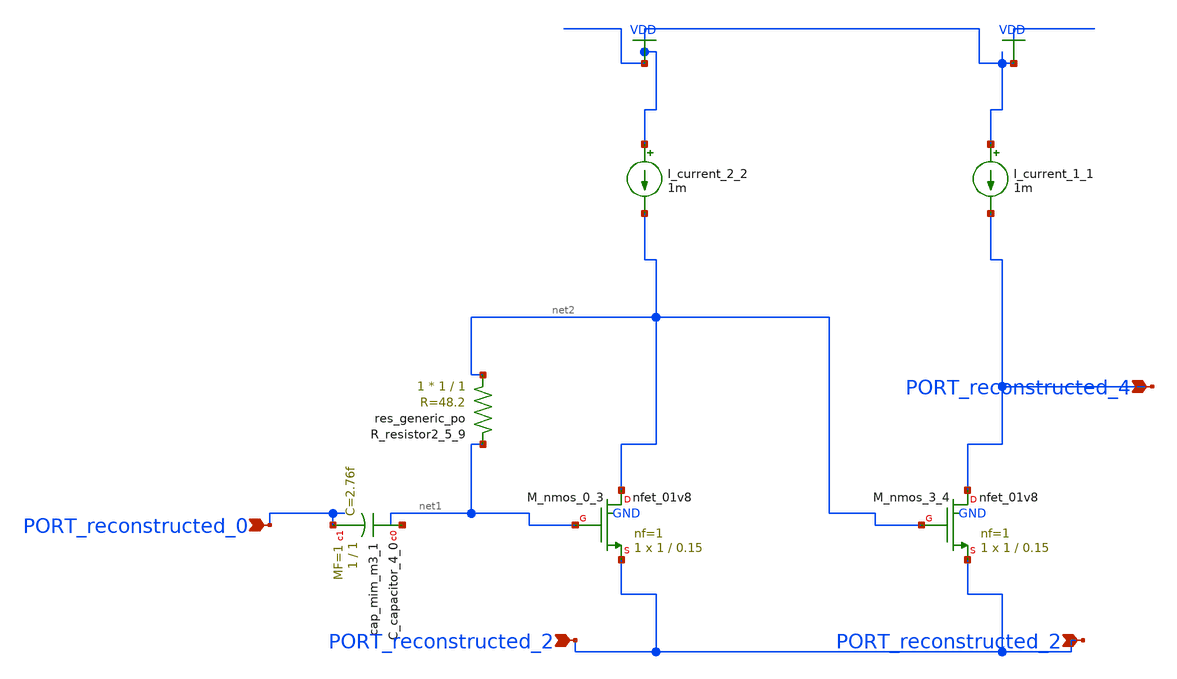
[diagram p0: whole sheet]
** sch_path: schematics/no_doi_01_006.sch
**.subckt no_doi_01_006 PORT_reconstructed_4 PORT_reconstructed_0 PORT_reconstructed_2
*+ PORT_reconstructed_2
*.ipin PORT_reconstructed_4
*.ipin PORT_reconstructed_0
*.ipin PORT_reconstructed_2
*.ipin PORT_reconstructed_2
XC_capacitor_4_0 net1 PORT_reconstructed_0 sky130_fd_pr__cap_mim_m3_1 W=1 L=1 MF=1 m=1
I_current_1_1 VDD PORT_reconstructed_4 1m
I_current_2_2 VDD net2 1m
XM_nmos_0_3 net2 net1 PORT_reconstructed_2 GND sky130_fd_pr__nfet_01v8 L=0.15 W=1 nf=1 ad='int((1 + 1)/2) * 1 / 1 * 0.29'
+ as='int((1 + 2)/2) * 1 / 1 * 0.29' pd='2*int((1 + 1)/2) * (1 / 1 + 0.29)' ps='2*int((1 + 2)/2) * (1 / 1 + 0.29)'
+ nrd='0.29 / 1 ' nrs='0.29 / 1 ' sa=0 sb=0 sd=0 mult=1 m=1
XM_nmos_3_4 PORT_reconstructed_4 net2 PORT_reconstructed_2 GND sky130_fd_pr__nfet_01v8 L=0.15 W=1 nf=1
+ ad='int((1 + 1)/2) * 1 / 1 * 0.29' as='int((1 + 2)/2) * 1 / 1 * 0.29' pd='2*int((1 + 1)/2) * (1 / 1 + 0.29)'
+ ps='2*int((1 + 2)/2) * (1 / 1 + 0.29)' nrd='0.29 / 1 ' nrs='0.29 / 1 ' sa=0 sb=0 sd=0 mult=1 m=1
XR_resistor2_5_9 net2 net1 sky130_fd_pr__res_generic_po W=1 L=1 m=1
**.ends
.GLOBAL VDD
.end
